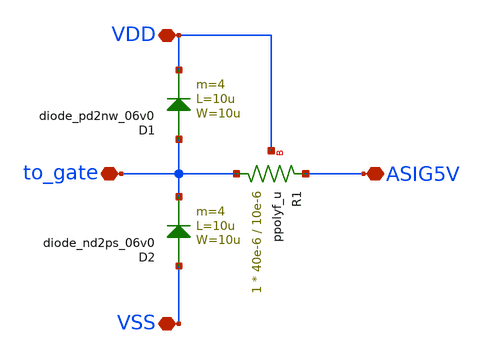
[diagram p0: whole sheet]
** sch_path: designs/Chipathon2025_pads/xschem/symbols/io_secondary_5p0/io_secondary_5p0.sch
**.subckt io_secondary_5p0 VSS VDD to_gate ASIG5V
*.iopin VSS
*.iopin VDD
*.iopin to_gate
*.iopin ASIG5V
D1 to_gate VDD diode_pd2nw_06v0 area='10u * 10u ' pj='2*10u + 2*10u ' m=4
XR1 to_gate ASIG5V VDD ppolyf_u r_width=40e-6 r_length=10e-6 m=1
D2 VSS to_gate diode_nd2ps_06v0 area='10u * 10u ' pj='2*10u + 2*10u ' m=4
**.ends
.end
